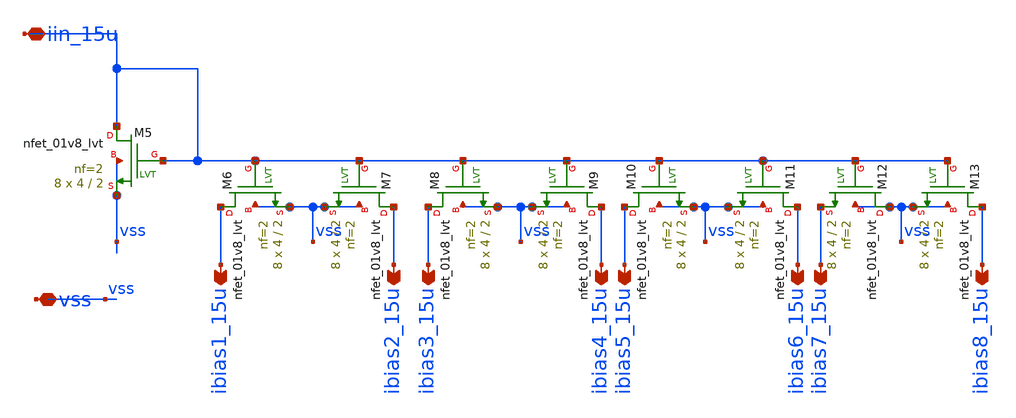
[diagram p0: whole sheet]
** sch_path: xschem/src/biasing_network/biasing_network.sch
**.subckt biasing_network iin_15u vss ibias1_15u ibias2_15u ibias3_15u ibias4_15u ibias5_15u
*+ ibias6_15u ibias7_15u ibias8_15u
*.iopin iin_15u
*.iopin vss
*.opin ibias1_15u
*.opin ibias2_15u
*.opin ibias3_15u
*.opin ibias4_15u
*.opin ibias5_15u
*.opin ibias6_15u
*.opin ibias7_15u
*.opin ibias8_15u
XM5 iin_15u iin_15u vss vss sky130_fd_pr__nfet_01v8_lvt L=2 W=4 nf=2 ad='int((nf+1)/2) * W/nf * 0.29'
+ as='int((nf+2)/2) * W/nf * 0.29' pd='2*int((nf+1)/2) * (W/nf + 0.29)' ps='2*int((nf+2)/2) * (W/nf + 0.29)'
+ nrd='0.29 / W' nrs='0.29 / W' sa=0 sb=0 sd=0 mult=8 m=8
XM6 ibias1_15u iin_15u vss vss sky130_fd_pr__nfet_01v8_lvt L=2 W=4 nf=2 ad='int((nf+1)/2) * W/nf * 0.29'
+ as='int((nf+2)/2) * W/nf * 0.29' pd='2*int((nf+1)/2) * (W/nf + 0.29)' ps='2*int((nf+2)/2) * (W/nf + 0.29)'
+ nrd='0.29 / W' nrs='0.29 / W' sa=0 sb=0 sd=0 mult=8 m=8
XM7 ibias2_15u iin_15u vss vss sky130_fd_pr__nfet_01v8_lvt L=2 W=4 nf=2 ad='int((nf+1)/2) * W/nf * 0.29'
+ as='int((nf+2)/2) * W/nf * 0.29' pd='2*int((nf+1)/2) * (W/nf + 0.29)' ps='2*int((nf+2)/2) * (W/nf + 0.29)'
+ nrd='0.29 / W' nrs='0.29 / W' sa=0 sb=0 sd=0 mult=8 m=8
XM8 ibias3_15u iin_15u vss vss sky130_fd_pr__nfet_01v8_lvt L=2 W=4 nf=2 ad='int((nf+1)/2) * W/nf * 0.29'
+ as='int((nf+2)/2) * W/nf * 0.29' pd='2*int((nf+1)/2) * (W/nf + 0.29)' ps='2*int((nf+2)/2) * (W/nf + 0.29)'
+ nrd='0.29 / W' nrs='0.29 / W' sa=0 sb=0 sd=0 mult=8 m=8
XM9 ibias4_15u iin_15u vss vss sky130_fd_pr__nfet_01v8_lvt L=2 W=4 nf=2 ad='int((nf+1)/2) * W/nf * 0.29'
+ as='int((nf+2)/2) * W/nf * 0.29' pd='2*int((nf+1)/2) * (W/nf + 0.29)' ps='2*int((nf+2)/2) * (W/nf + 0.29)'
+ nrd='0.29 / W' nrs='0.29 / W' sa=0 sb=0 sd=0 mult=8 m=8
XM10 ibias5_15u iin_15u vss vss sky130_fd_pr__nfet_01v8_lvt L=2 W=4 nf=2 ad='int((nf+1)/2) * W/nf * 0.29'
+ as='int((nf+2)/2) * W/nf * 0.29' pd='2*int((nf+1)/2) * (W/nf + 0.29)' ps='2*int((nf+2)/2) * (W/nf + 0.29)'
+ nrd='0.29 / W' nrs='0.29 / W' sa=0 sb=0 sd=0 mult=8 m=8
XM11 ibias6_15u iin_15u vss vss sky130_fd_pr__nfet_01v8_lvt L=2 W=4 nf=2 ad='int((nf+1)/2) * W/nf * 0.29'
+ as='int((nf+2)/2) * W/nf * 0.29' pd='2*int((nf+1)/2) * (W/nf + 0.29)' ps='2*int((nf+2)/2) * (W/nf + 0.29)'
+ nrd='0.29 / W' nrs='0.29 / W' sa=0 sb=0 sd=0 mult=8 m=8
XM12 vss iin_15u ibias7_15u vss sky130_fd_pr__nfet_01v8_lvt L=2 W=4 nf=2 ad='int((nf+1)/2) * W/nf * 0.29'
+ as='int((nf+2)/2) * W/nf * 0.29' pd='2*int((nf+1)/2) * (W/nf + 0.29)' ps='2*int((nf+2)/2) * (W/nf + 0.29)'
+ nrd='0.29 / W' nrs='0.29 / W' sa=0 sb=0 sd=0 mult=8 m=8
XM13 ibias8_15u iin_15u vss vss sky130_fd_pr__nfet_01v8_lvt L=2 W=4 nf=2 ad='int((nf+1)/2) * W/nf * 0.29'
+ as='int((nf+2)/2) * W/nf * 0.29' pd='2*int((nf+1)/2) * (W/nf + 0.29)' ps='2*int((nf+2)/2) * (W/nf + 0.29)'
+ nrd='0.29 / W' nrs='0.29 / W' sa=0 sb=0 sd=0 mult=8 m=8
**.ends
.end
